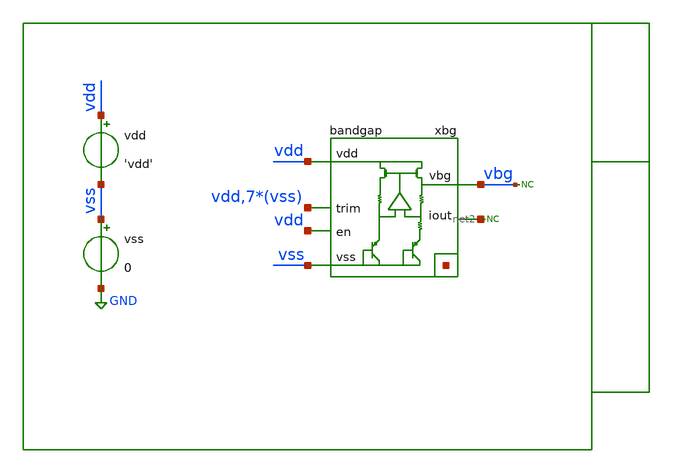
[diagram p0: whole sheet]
** sch_path: xschem/tb/bandgap_cm/bandgap/op_bandgap_power.sch
**.subckt op_bandgap_power
xbg vdd vbg vss net1[7] net1[6] net1[5] net1[4] net1[3] net1[2] net1[1] net1[0] vdd vss vss vss vss
+ vss vss vss net2 vdd bandgap
vdd vdd vss 'vdd'
vss vss GND 0
* noconn vbg
* noconn #net2
**** begin user architecture code

* Control

.param vdd = 3.3
.temp 27
.options reltol     = 1e-6

*------------------------------------------------------------
* Save device current for OP analysis
*------------------------------------------------------------
.save @m.xbg.xm1.m0[id]
.save @m.xbg.xm2.m0[id]
.save @m.xbg.xamp.xmb1.m0[id]
.save @m.xbg.xamp.xmb2.m0[id]
.save @m.xbg.xamp.xmt1.m0[id]
.save @m.xbg.xamp.xmc7.m0[id]
.save @m.xbg.xamp.xmc8.m0[id]

.control
save all

op

let vsup = v(vdd)
let itot = abs(vdd#branch)

let id_xm1  = abs(@m.xbg.xm1.m0[id])
let id_xm2  = abs(@m.xbg.xm2.m0[id])
let id_xmb1 = abs(@m.xbg.xamp.xmb1.m0[id])
let id_xmb2 = abs(@m.xbg.xamp.xmb2.m0[id])
let id_xmt1 = abs(@m.xbg.xamp.xmt1.m0[id])
let id_xmc7 = abs(@m.xbg.xamp.xmc7.m0[id])
let id_xmc8 = abs(@m.xbg.xamp.xmc8.m0[id])

let iamp = id_xmb1 + id_xmb2 + id_xmt1 + id_xmc7 + id_xmc8
let ibgc = id_xm1 + id_xm2
let isum = iamp + ibgc

let pamp = vsup*iamp
let pbgc = vsup*ibgc
let psum = vsup*isum
let ptot = vsup*itot

print iamp
print ibgc
print itot

print pamp
print pbgc
print ptot

.endc
.end


 * Model Corners

.include $::CORNERS/ngspice/tt.spice
*.include $::CORNERS/ngspice/ff.spice
*.include $::CORNERS/ngspice/ss.spice
*.include $::CORNERS/ngspice/sf.spice
*.include $::CORNERS/ngspice/fs.spice

**** end user architecture code
**.ends
.GLOBAL GND
.end
